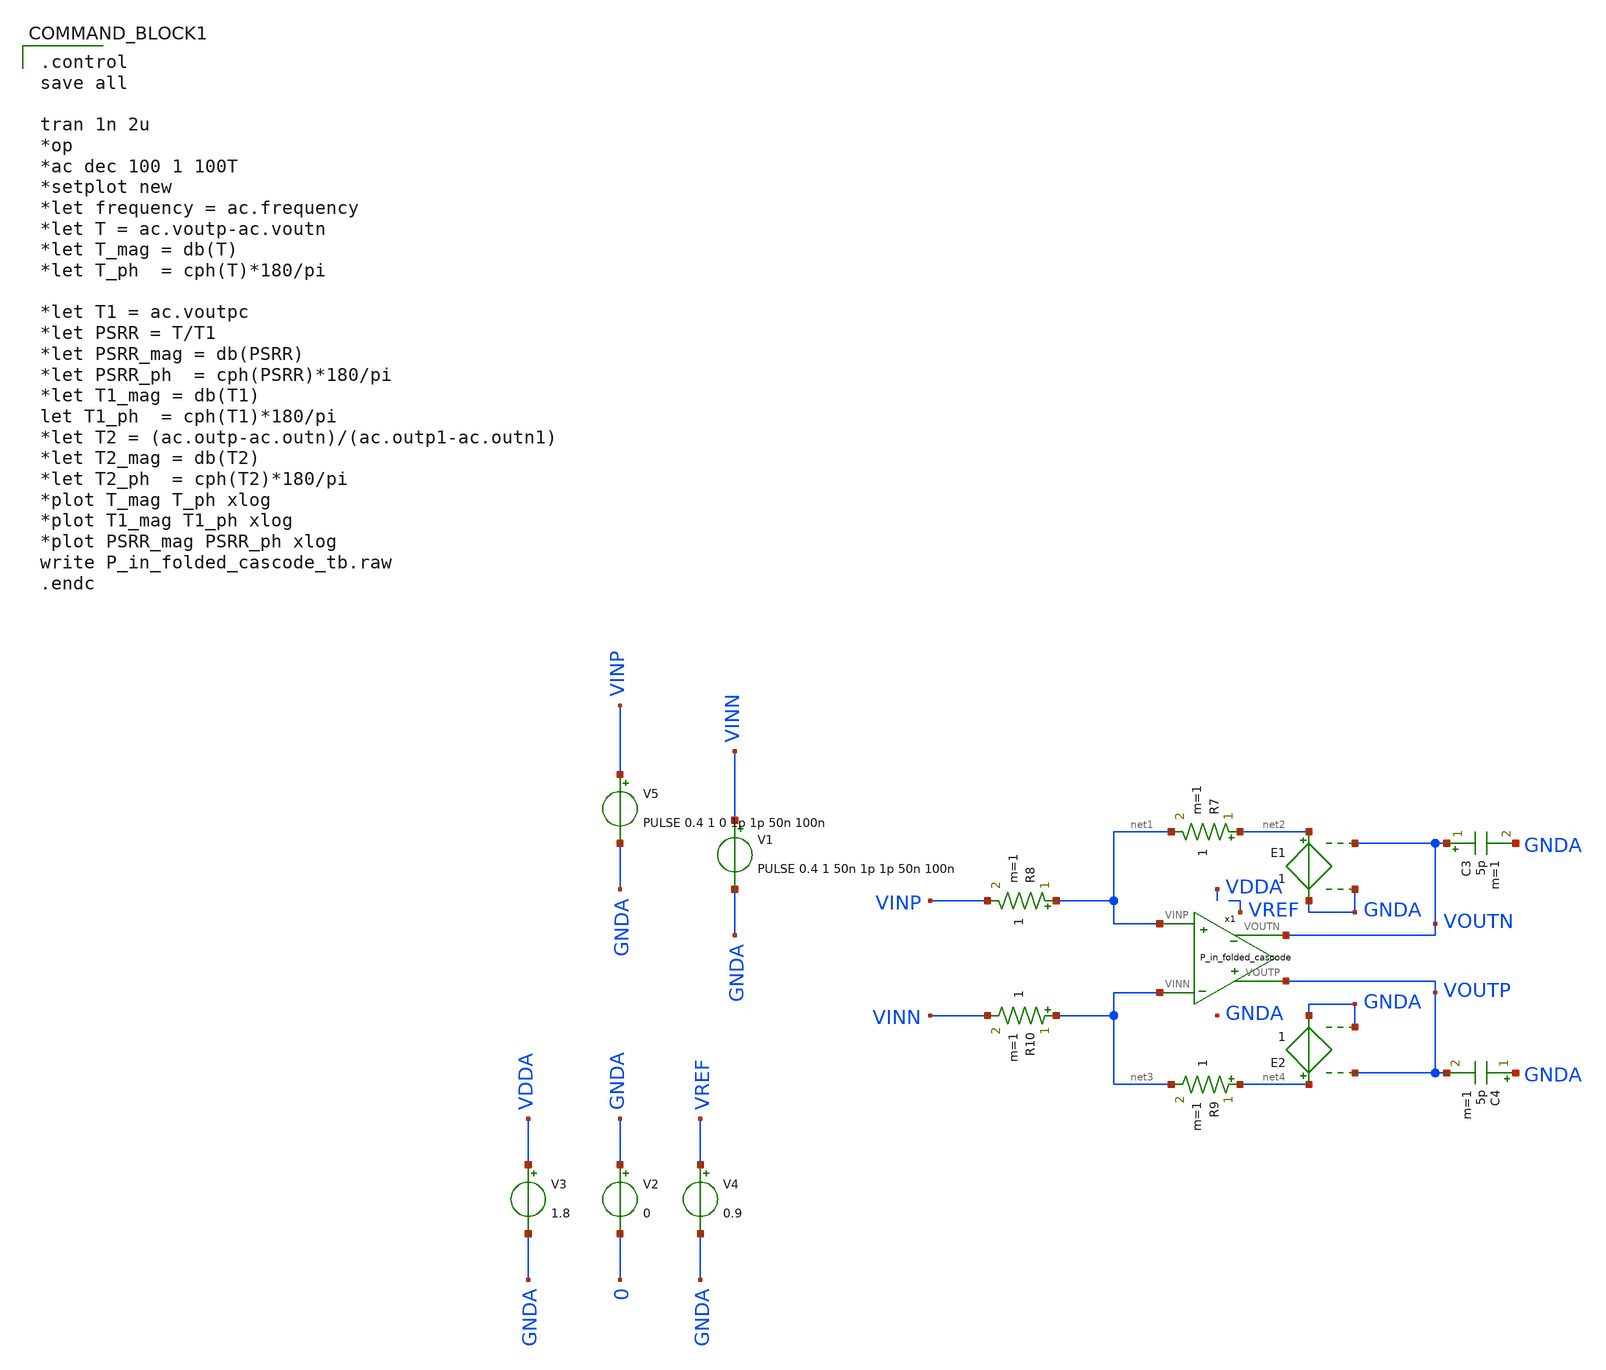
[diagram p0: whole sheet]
** sch_path: P_in_folded_cascode_tb.sch
**.subckt P_in_folded_cascode_tb
C3 VOUTN GNDA 5p m=1
C4 GNDA VOUTP 5p m=1
R7 net2 net1 1 m=1
R8 net1 VINP 1 m=1
R9 net4 net3 1 m=1
R10 net3 VINN 1 m=1
E1 net2 GNDA VOUTN GNDA 1
E2 net4 GNDA VOUTP GNDA 1
V2 GNDA 0 0
V5 VINP GNDA PULSE 0.4 1 0 1p 1p 50n 100n
V1 VINN GNDA PULSE 0.4 1 50n 1p 1p 50n 100n
x1 net1 net3 VOUTN VOUTP P_in_folded_cascode
V3 VDDA GNDA 1.8
V4 VREF GNDA 0.9
**** begin user architecture code

.control
save all

tran 1n 2u
*op
*ac dec 100 1 100T
*setplot new
*let frequency = ac.frequency
*let T = ac.voutp-ac.voutn
*let T_mag = db(T)
*let T_ph  = cph(T)*180/pi

*let T1 = ac.voutpc
*let PSRR = T/T1
*let PSRR_mag = db(PSRR)
*let PSRR_ph  = cph(PSRR)*180/pi
*let T1_mag = db(T1)
let T1_ph  = cph(T1)*180/pi
*let T2 = (ac.outp-ac.outn)/(ac.outp1-ac.outn1)
*let T2_mag = db(T2)
*let T2_ph  = cph(T2)*180/pi
*plot T_mag T_ph xlog
*plot T1_mag T1_ph xlog
*plot PSRR_mag PSRR_ph xlog
write P_in_folded_cascode_tb.raw
.endc


** opencircuitdesign pdks install
.lib $::SKYWATER_MODELS/sky130.lib.spice ff


**** end user architecture code
**.ends

* expanding   symbol:  P_in_folded_cascode.sym # of pins=4
** sym_path: P_in_folded_cascode.sym
** sch_path: P_in_folded_cascode.sch
.subckt P_in_folded_cascode VINP VINN VOUTN VOUTP
*.ipin VINP
*.ipin VINN
*.opin VOUTN
*.opin VOUTP
XM4 net1 VCMFB VDDA VDDA sky130_fd_pr__pfet_01v8_lvt L=0.7 W=11 nf=1 ad='int((nf+1)/2) * W/nf * 0.29'
+ as='int((nf+2)/2) * W/nf * 0.29' pd='2*int((nf+1)/2) * (W/nf + 0.29)' ps='2*int((nf+2)/2) * (W/nf + 0.29)'
+ nrd='0.29 / W' nrs='0.29 / W' sa=0 sb=0 sd=0 mult=60 m=60
XM5 net2 VCMFB VDDA VDDA sky130_fd_pr__pfet_01v8_lvt L=0.7 W=11 nf=1 ad='int((nf+1)/2) * W/nf * 0.29'
+ as='int((nf+2)/2) * W/nf * 0.29' pd='2*int((nf+1)/2) * (W/nf + 0.29)' ps='2*int((nf+2)/2) * (W/nf + 0.29)'
+ nrd='0.29 / W' nrs='0.29 / W' sa=0 sb=0 sd=0 mult=60 m=60
XM6 VOUTPF VB2 net1 VDDA sky130_fd_pr__pfet_01v8_lvt L=0.7 W=11.5 nf=1 ad='int((nf+1)/2) * W/nf * 0.29'
+ as='int((nf+2)/2) * W/nf * 0.29' pd='2*int((nf+1)/2) * (W/nf + 0.29)' ps='2*int((nf+2)/2) * (W/nf + 0.29)'
+ nrd='0.29 / W' nrs='0.29 / W' sa=0 sb=0 sd=0 mult=10 m=10
XM7 VOUTNF VB2 net2 VDDA sky130_fd_pr__pfet_01v8_lvt L=0.7 W=11.5 nf=1 ad='int((nf+1)/2) * W/nf * 0.29'
+ as='int((nf+2)/2) * W/nf * 0.29' pd='2*int((nf+1)/2) * (W/nf + 0.29)' ps='2*int((nf+2)/2) * (W/nf + 0.29)'
+ nrd='0.29 / W' nrs='0.29 / W' sa=0 sb=0 sd=0 mult=10 m=10
XM8 VOUTPF VB3 net3 GNDA sky130_fd_pr__nfet_01v8_lvt L=0.7 W=3.7 nf=1 ad='int((nf+1)/2) * W/nf * 0.29'
+ as='int((nf+2)/2) * W/nf * 0.29' pd='2*int((nf+1)/2) * (W/nf + 0.29)' ps='2*int((nf+2)/2) * (W/nf + 0.29)'
+ nrd='0.29 / W' nrs='0.29 / W' sa=0 sb=0 sd=0 mult=5 m=5
XM9 VOUTNF VB3 net4 GNDA sky130_fd_pr__nfet_01v8_lvt L=0.7 W=3.7 nf=1 ad='int((nf+1)/2) * W/nf * 0.29'
+ as='int((nf+2)/2) * W/nf * 0.29' pd='2*int((nf+1)/2) * (W/nf + 0.29)' ps='2*int((nf+2)/2) * (W/nf + 0.29)'
+ nrd='0.29 / W' nrs='0.29 / W' sa=0 sb=0 sd=0 mult=5 m=5
XM10 net3 VB4 net5 GNDA sky130_fd_pr__nfet_01v8_lvt L=0.7 W=2.5 nf=1 ad='int((nf+1)/2) * W/nf * 0.29'
+ as='int((nf+2)/2) * W/nf * 0.29' pd='2*int((nf+1)/2) * (W/nf + 0.29)' ps='2*int((nf+2)/2) * (W/nf + 0.29)'
+ nrd='0.29 / W' nrs='0.29 / W' sa=0 sb=0 sd=0 mult=9 m=9
XM11 net4 VB4 net5 GNDA sky130_fd_pr__nfet_01v8_lvt L=0.7 W=2.5 nf=1 ad='int((nf+1)/2) * W/nf * 0.29'
+ as='int((nf+2)/2) * W/nf * 0.29' pd='2*int((nf+1)/2) * (W/nf + 0.29)' ps='2*int((nf+2)/2) * (W/nf + 0.29)'
+ nrd='0.29 / W' nrs='0.29 / W' sa=0 sb=0 sd=0 mult=9 m=9
XM12 net6 VB1 VDDA VDDA sky130_fd_pr__pfet_01v8_lvt L=0.7 W=9.5 nf=1 ad='int((nf+1)/2) * W/nf * 0.29'
+ as='int((nf+2)/2) * W/nf * 0.29' pd='2*int((nf+1)/2) * (W/nf + 0.29)' ps='2*int((nf+2)/2) * (W/nf + 0.29)'
+ nrd='0.29 / W' nrs='0.29 / W' sa=0 sb=0 sd=0 mult=40 m=40
XM15 VB1 VB2 net6 VDDA sky130_fd_pr__pfet_01v8_lvt L=0.7 W=11.5 nf=1 ad='int((nf+1)/2) * W/nf * 0.29'
+ as='int((nf+2)/2) * W/nf * 0.29' pd='2*int((nf+1)/2) * (W/nf + 0.29)' ps='2*int((nf+2)/2) * (W/nf + 0.29)'
+ nrd='0.29 / W' nrs='0.29 / W' sa=0 sb=0 sd=0 mult=10 m=10
.save v(vb1)
.save v(net6)
R1 VB1 VB2 2.5k m=1
.save v(vb2)
XM13 net7 VB4 net5 net5 sky130_fd_pr__nfet_01v8_lvt L=0.7 W=2.5 nf=1 ad='int((nf+1)/2) * W/nf * 0.29'
+ as='int((nf+2)/2) * W/nf * 0.29' pd='2*int((nf+1)/2) * (W/nf + 0.29)' ps='2*int((nf+2)/2) * (W/nf + 0.29)'
+ nrd='0.29 / W' nrs='0.29 / W' sa=0 sb=0 sd=0 mult=5 m=5
XM14 net8 VB4 net5 net5 sky130_fd_pr__nfet_01v8_lvt L=0.7 W=2.5 nf=1 ad='int((nf+1)/2) * W/nf * 0.29'
+ as='int((nf+2)/2) * W/nf * 0.29' pd='2*int((nf+1)/2) * (W/nf + 0.29)' ps='2*int((nf+2)/2) * (W/nf + 0.29)'
+ nrd='0.29 / W' nrs='0.29 / W' sa=0 sb=0 sd=0 mult=5 m=5
XM16 VB4 VB3 net7 net5 sky130_fd_pr__nfet_01v8_lvt L=0.7 W=3.7 nf=1 ad='int((nf+1)/2) * W/nf * 0.29'
+ as='int((nf+2)/2) * W/nf * 0.29' pd='2*int((nf+1)/2) * (W/nf + 0.29)' ps='2*int((nf+2)/2) * (W/nf + 0.29)'
+ nrd='0.29 / W' nrs='0.29 / W' sa=0 sb=0 sd=0 mult=5 m=5
XM17 VB2 VB3 net8 net5 sky130_fd_pr__nfet_01v8_lvt L=0.7 W=3.7 nf=1 ad='int((nf+1)/2) * W/nf * 0.29'
+ as='int((nf+2)/2) * W/nf * 0.29' pd='2*int((nf+1)/2) * (W/nf + 0.29)' ps='2*int((nf+2)/2) * (W/nf + 0.29)'
+ nrd='0.29 / W' nrs='0.29 / W' sa=0 sb=0 sd=0 mult=5 m=5
.save v(net7)
.save v(net8)
.save v(vb4)
R2 VB3 VB4 2k m=1
I0 VDDA VB3 200u
XM18 VOUTN VOUTPF net5 net5 sky130_fd_pr__nfet_01v8_lvt L=0.7 W=14.8 nf=1 ad='int((nf+1)/2) * W/nf * 0.29'
+ as='int((nf+2)/2) * W/nf * 0.29' pd='2*int((nf+1)/2) * (W/nf + 0.29)' ps='2*int((nf+2)/2) * (W/nf + 0.29)'
+ nrd='0.29 / W' nrs='0.29 / W' sa=0 sb=0 sd=0 mult=21 m=21
XM19 VOUTN net9 VDDA VDDA sky130_fd_pr__pfet_01v8_lvt L=0.7 W=8 nf=1 ad='int((nf+1)/2) * W/nf * 0.29'
+ as='int((nf+2)/2) * W/nf * 0.29' pd='2*int((nf+1)/2) * (W/nf + 0.29)' ps='2*int((nf+2)/2) * (W/nf + 0.29)'
+ nrd='0.29 / W' nrs='0.29 / W' sa=0 sb=0 sd=0 mult=66 m=66
XM20 VOUTP VOUTNF net5 net5 sky130_fd_pr__nfet_01v8_lvt L=0.7 W=14.8 nf=1 ad='int((nf+1)/2) * W/nf * 0.29'
+ as='int((nf+2)/2) * W/nf * 0.29' pd='2*int((nf+1)/2) * (W/nf + 0.29)' ps='2*int((nf+2)/2) * (W/nf + 0.29)'
+ nrd='0.29 / W' nrs='0.29 / W' sa=0 sb=0 sd=0 mult=21 m=21
XM21 VOUTP net9 VDDA VDDA sky130_fd_pr__pfet_01v8_lvt L=0.7 W=8 nf=1 ad='int((nf+1)/2) * W/nf * 0.29'
+ as='int((nf+2)/2) * W/nf * 0.29' pd='2*int((nf+1)/2) * (W/nf + 0.29)' ps='2*int((nf+2)/2) * (W/nf + 0.29)'
+ nrd='0.29 / W' nrs='0.29 / W' sa=0 sb=0 sd=0 mult=66 m=66
R5 net10 VOUTPF 100 m=1
R6 net11 VOUTNF 100 m=1
C1 VOUTN net10 1.1p m=1
C2 VOUTP net11 1.1p m=1
V2 GNDA 0 0
V3 VDDA GNDA 1.8
V4 VREF GNDA 0.9
.save v(net1)
.save v(net2)
.save v(voutpf)
.save v(voutnf)
.save v(net3)
.save v(net4)
.save v(voutn)
.save v(voutp)
.save v(vb3)
XM1 net12 VB1 VDDA VDDA sky130_fd_pr__pfet_01v8_lvt L=0.7 W=9.5 nf=1 ad='int((nf+1)/2) * W/nf * 0.29'
+ as='int((nf+2)/2) * W/nf * 0.29' pd='2*int((nf+1)/2) * (W/nf + 0.29)' ps='2*int((nf+2)/2) * (W/nf + 0.29)'
+ nrd='0.29 / W' nrs='0.29 / W' sa=0 sb=0 sd=0 mult=58 m=58
XM2 net3 VINN net12 VDDA sky130_fd_pr__pfet_01v8_lvt L=0.7 W=10.8 nf=1 ad='int((nf+1)/2) * W/nf * 0.29'
+ as='int((nf+2)/2) * W/nf * 0.29' pd='2*int((nf+1)/2) * (W/nf + 0.29)' ps='2*int((nf+2)/2) * (W/nf + 0.29)'
+ nrd='0.29 / W' nrs='0.29 / W' sa=0 sb=0 sd=0 mult=20 m=20
XM3 net12 VINP net4 VDDA sky130_fd_pr__pfet_01v8_lvt L=0.7 W=10.8 nf=1 ad='int((nf+1)/2) * W/nf * 0.29'
+ as='int((nf+2)/2) * W/nf * 0.29' pd='2*int((nf+1)/2) * (W/nf + 0.29)' ps='2*int((nf+2)/2) * (W/nf + 0.29)'
+ nrd='0.29 / W' nrs='0.29 / W' sa=0 sb=0 sd=0 mult=20 m=20
R3 net9 VOUTN 100Meg m=1
R4 VOUTP net9 100Meg m=1
XM22 net13 VB4 net5 net5 sky130_fd_pr__nfet_01v8_lvt L=0.7 W=2.5 nf=1 ad='int((nf+1)/2) * W/nf * 0.29'
+ as='int((nf+2)/2) * W/nf * 0.29' pd='2*int((nf+1)/2) * (W/nf + 0.29)' ps='2*int((nf+2)/2) * (W/nf + 0.29)'
+ nrd='0.29 / W' nrs='0.29 / W' sa=0 sb=0 sd=0 mult=1 m=1
XM23 net14 VB4 net5 net5 sky130_fd_pr__nfet_01v8_lvt L=0.7 W=2.5 nf=1 ad='int((nf+1)/2) * W/nf * 0.29'
+ as='int((nf+2)/2) * W/nf * 0.29' pd='2*int((nf+1)/2) * (W/nf + 0.29)' ps='2*int((nf+2)/2) * (W/nf + 0.29)'
+ nrd='0.29 / W' nrs='0.29 / W' sa=0 sb=0 sd=0 mult=1 m=1
XM24 VCMFB VREF net13 GNDA sky130_fd_pr__nfet_01v8_lvt L=0.7 W=14.1 nf=1 ad='int((nf+1)/2) * W/nf * 0.29'
+ as='int((nf+2)/2) * W/nf * 0.29' pd='2*int((nf+1)/2) * (W/nf + 0.29)' ps='2*int((nf+2)/2) * (W/nf + 0.29)'
+ nrd='0.29 / W' nrs='0.29 / W' sa=0 sb=0 sd=0 mult=1 m=1
XM25 VCMFB VREF net14 GNDA sky130_fd_pr__nfet_01v8_lvt L=0.7 W=14.1 nf=1 ad='int((nf+1)/2) * W/nf * 0.29'
+ as='int((nf+2)/2) * W/nf * 0.29' pd='2*int((nf+1)/2) * (W/nf + 0.29)' ps='2*int((nf+2)/2) * (W/nf + 0.29)'
+ nrd='0.29 / W' nrs='0.29 / W' sa=0 sb=0 sd=0 mult=1 m=1
XM26 net15 VOUTPF net13 GNDA sky130_fd_pr__nfet_01v8_lvt L=0.7 W=14.1 nf=1 ad='int((nf+1)/2) * W/nf * 0.29'
+ as='int((nf+2)/2) * W/nf * 0.29' pd='2*int((nf+1)/2) * (W/nf + 0.29)' ps='2*int((nf+2)/2) * (W/nf + 0.29)'
+ nrd='0.29 / W' nrs='0.29 / W' sa=0 sb=0 sd=0 mult=1 m=1
XM27 net15 VOUTNF net14 GNDA sky130_fd_pr__nfet_01v8_lvt L=0.7 W=14.1 nf=1 ad='int((nf+1)/2) * W/nf * 0.29'
+ as='int((nf+2)/2) * W/nf * 0.29' pd='2*int((nf+1)/2) * (W/nf + 0.29)' ps='2*int((nf+2)/2) * (W/nf + 0.29)'
+ nrd='0.29 / W' nrs='0.29 / W' sa=0 sb=0 sd=0 mult=1 m=1
XM28 VCMFB VCMFB VDDA VDDA sky130_fd_pr__pfet_01v8_lvt L=0.7 W=11 nf=1 ad='int((nf+1)/2) * W/nf * 0.29'
+ as='int((nf+2)/2) * W/nf * 0.29' pd='2*int((nf+1)/2) * (W/nf + 0.29)' ps='2*int((nf+2)/2) * (W/nf + 0.29)'
+ nrd='0.29 / W' nrs='0.29 / W' sa=0 sb=0 sd=0 mult=10 m=10
XM29 net15 net15 VDDA VDDA sky130_fd_pr__pfet_01v8_lvt L=0.7 W=11 nf=1 ad='int((nf+1)/2) * W/nf * 0.29'
+ as='int((nf+2)/2) * W/nf * 0.29' pd='2*int((nf+1)/2) * (W/nf + 0.29)' ps='2*int((nf+2)/2) * (W/nf + 0.29)'
+ nrd='0.29 / W' nrs='0.29 / W' sa=0 sb=0 sd=0 mult=10 m=10
.save v(net13)
.save v(net14)
.save v(vcmfb)
.save v(net15)
.save v(net9)
C7 VOUTP GNDA 5p m=1
C8 VOUTN GNDA 5p m=1
Vmeas net5 GNDA 0
.save i(vmeas)
.ends

.end
